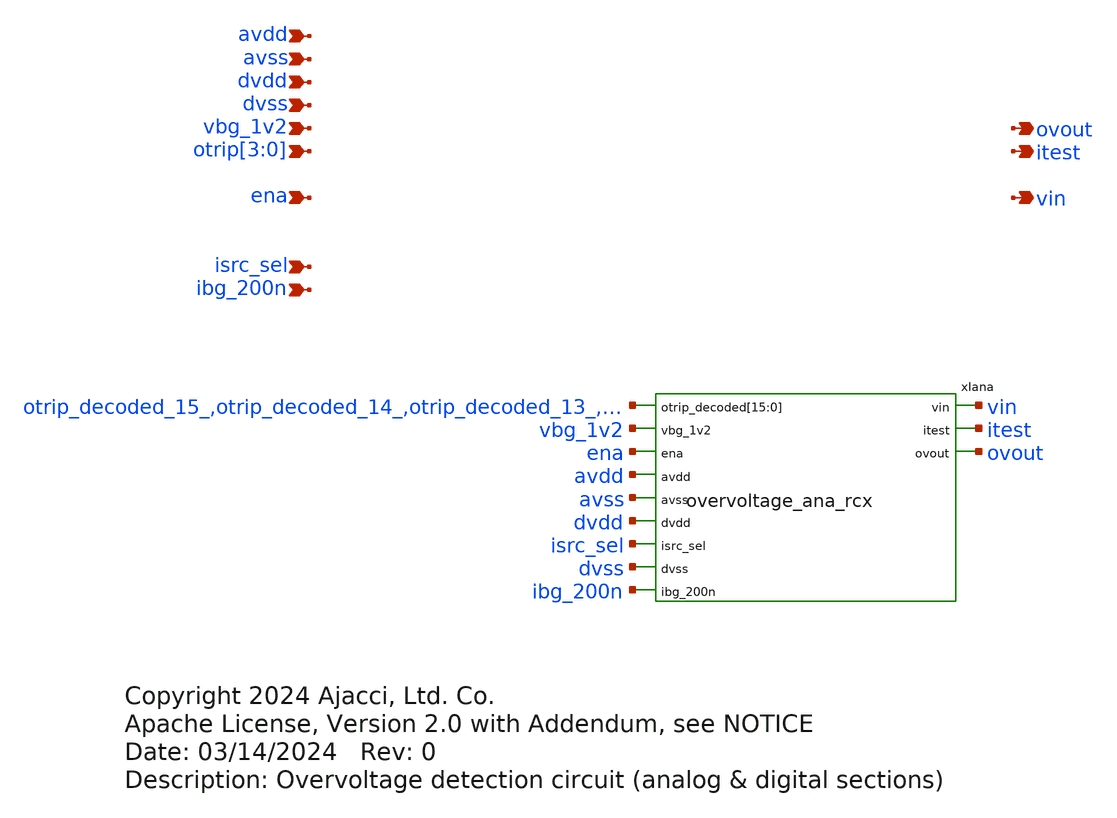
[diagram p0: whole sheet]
** sch_path: xschem/sky130_ajc_ip__overvoltage.sch
* Copyright 2024 Ajacci, Ltd. Co.
* Apache License, Version 2.0 with Addendum, see NOTICE
**.subckt sky130_ajc_ip__overvoltage avdd avss dvdd dvss vbg_1v2 otrip[3],otrip[2],otrip[1],otrip[0]
*+ ena isrc_sel ibg_200n vin ovout itest
*.ipin avdd
*.ipin avss
*.ipin dvdd
*.ipin dvss
*.ipin vbg_1v2
*.ipin otrip[3],otrip[2],otrip[1],otrip[0]
*.ipin ena
*.ipin isrc_sel
*.ipin ibg_200n
*.opin vin
*.opin ovout
*.opin itest
xIana otrip_decoded_15_ otrip_decoded_14_ otrip_decoded_13_ otrip_decoded_12_ otrip_decoded_11_
+ otrip_decoded_10_ otrip_decoded_9_ otrip_decoded_8_ otrip_decoded_7_ otrip_decoded_6_ otrip_decoded_5_
+ otrip_decoded_4_ otrip_decoded_3_ otrip_decoded_2_ otrip_decoded_1_ otrip_decoded_0_ vbg_1v2 ena avdd avss dvdd
+ isrc_sel dvss vin itest ibg_200n ovout overvoltage_ana_rcx
**** begin user architecture code



*XSPICE CO-SIM netlist
.include overvoltage_dig.out.spice

r0 otrip[0] otrip0 1
r1 otrip[1] otrip1 1
r2 otrip[2] otrip2 1
r3 otrip[3] otrip3 1

xiovervoltage_dig dvss dvdd  otrip0 otrip1 otrip2 otrip3 otrip_decoded_0_  otrip_decoded_10_
+ otrip_decoded_11_ otrip_decoded_12_ otrip_decoded_13_ otrip_decoded_14_ otrip_decoded_15_ otrip_decoded_1_
+ otrip_decoded_2_ otrip_decoded_3_ otrip_decoded_4_ otrip_decoded_5_ otrip_decoded_6_ otrip_decoded_7_
+ otrip_decoded_8_ otrip_decoded_9_  overvoltage_dig



**** end user architecture code
**.ends

* expanding   symbol:  xschem/overvoltage_ana_rcx.sym # of pins=12
** sym_path: xschem/overvoltage_ana_rcx.sym
** sch_path: xschem/overvoltage_ana_rcx.sch
.subckt overvoltage_ana_rcx otrip_decoded[15] otrip_decoded[14] otrip_decoded[13] otrip_decoded[12]
+ otrip_decoded[11] otrip_decoded[10] otrip_decoded[9] otrip_decoded[8] otrip_decoded[7] otrip_decoded[6]
+ otrip_decoded[5] otrip_decoded[4] otrip_decoded[3] otrip_decoded[2] otrip_decoded[1] otrip_decoded[0] vbg_1v2 ena
+ avdd avss dvdd isrc_sel dvss vin itest ibg_200n ovout
*.ipin vbg_1v2
*.ipin avdd
*.ipin avss
*.ipin dvdd
*.ipin dvss
*.ipin ena
*.ipin isrc_sel
*.ipin ibg_200n
*.opin ovout
*.opin itest
*.ipin
*+ otrip_decoded[15],otrip_decoded[14],otrip_decoded[13],otrip_decoded[12],otrip_decoded[11],otrip_decoded[10],otrip_decoded[9],otrip_decoded[8],otrip_decoded[7],otrip_decoded[6],otrip_decoded[5],otrip_decoded[4],otrip_decoded[3],otrip_decoded[2],otrip_decoded[1],otrip_decoded[0]
*.opin vin
**** begin user architecture code



.include mag/rcx/overvoltage_ana_rcx.spice

xIana otrip_decoded[14] otrip_decoded[13] otrip_decoded[11]  otrip_decoded[10] otrip_decoded[1]
+ otrip_decoded[0] ena itest ibg_200n otrip_decoded[7]  otrip_decoded[4] vbg_1v2 vin isrc_sel otrip_decoded[5]
+ otrip_decoded[8] otrip_decoded[2]  ovout otrip_decoded[15] otrip_decoded[9] otrip_decoded[12] otrip_decoded[3]
+ otrip_decoded[6]  avss dvdd dvss avdd overvoltage_ana_rcx


**** end user architecture code
.ends

.end
